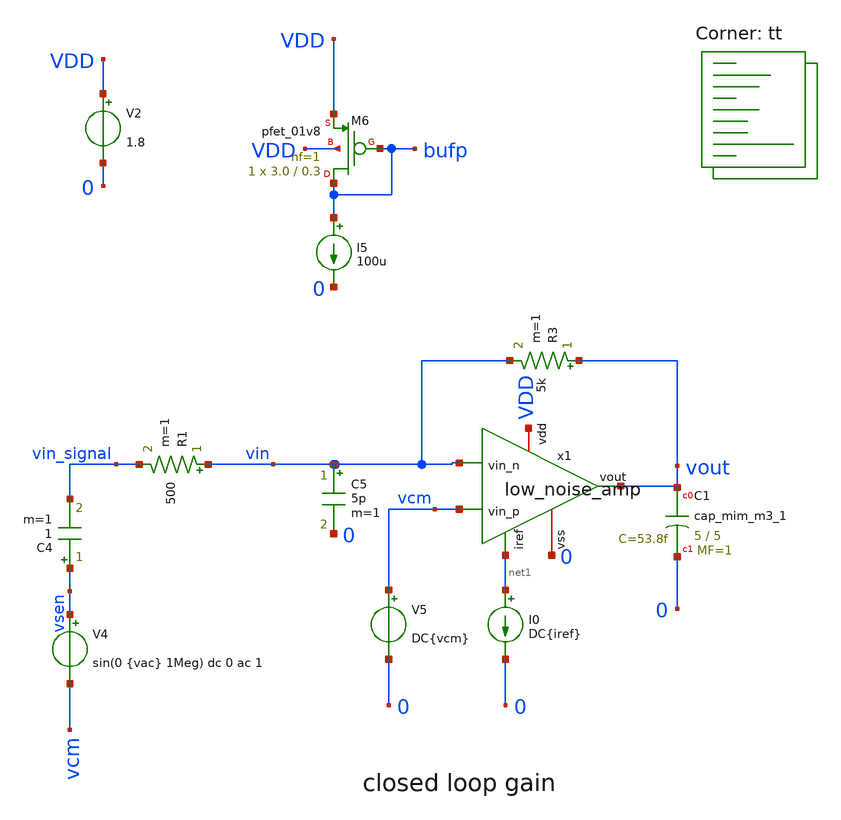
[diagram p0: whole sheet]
** sch_path: design/xschem/low_noise_amp_closed_loop_tb.sch
**.subckt low_noise_amp_closed_loop_tb
V2 VDD 0 1.8
XM6 bufp bufp VDD VDD sky130_fd_pr__pfet_01v8 L=0.3 W=3.0 nf=1 ad='int((nf+1)/2) * W/nf * 0.29' as='int((nf+2)/2) * W/nf * 0.29'
+ pd='2*int((nf+1)/2) * (W/nf + 0.29)' ps='2*int((nf+2)/2) * (W/nf + 0.29)' nrd='0.29 / W' nrs='0.29 / W'
+ sa=0 sb=0 sd=0 mult=1 m=1
I5 bufp 0 100u
XC1 net2 0 sky130_fd_pr__cap_mim_m3_1 W=5 L=5 MF=1 m=1
x1 VDD net1 vin vcm vout 0 low_noise_amp
C5 vin 0 5p m=1
V5 vcm 0 DC{vcm}
V4 vsen vcm sin(0 {vac} 1Meg) dc 0 ac 1
C4 vsen vin_signal 1 m=1
R1 vin vin_signal 500 m=1
R3 vout vin 5k m=1
I0 net1 0 DC{iref}
**** begin user architecture code
.lib $::SKYWATER_MODELS/sky130.lib.spice tt




* Circuit Parameters
.param iref = 100u
.param vdd  = 1.8
.param vss  = 0.0
.param vcm  = 0.8
.param vac  = 10m
.options TEMP = 65.0


* OP Parameters & Singals to save
.save all  @M.X1.XM1.msky130_fd_pr__pfet_01v8[id] @M.X1.XM1.msky130_fd_pr__pfet_01v8[vth] @M.X1.XM1.msky130_fd_pr__pfet_01v8[vgs] @M.X1.XM1.msky130_fd_pr__pfet_01v8[vds] @M.X1.XM1.msky130_fd_pr__pfet_01v8[vdsat] @M.X1.XM1.msky130_fd_pr__pfet_01v8[gm] @M.X1.XM1.msky130_fd_pr__pfet_01v8[gds]  @M.X1.XM2.msky130_fd_pr__pfet_01v8[id] @M.X1.XM2.msky130_fd_pr__pfet_01v8[vth] @M.X1.XM2.msky130_fd_pr__pfet_01v8[vgs] @M.X1.XM2.msky130_fd_pr__pfet_01v8[vds] @M.X1.XM2.msky130_fd_pr__pfet_01v8[vdsat] @M.X1.XM2.msky130_fd_pr__pfet_01v8[gm] @M.X1.XM2.msky130_fd_pr__pfet_01v8[gds]  @M.X1.XM3.msky130_fd_pr__nfet_01v8[id] @M.X1.XM3.msky130_fd_pr__nfet_01v8[vth] @M.X1.XM3.msky130_fd_pr__nfet_01v8[vgs] @M.X1.XM3.msky130_fd_pr__nfet_01v8[vds] @M.X1.XM3.msky130_fd_pr__nfet_01v8[vdsat] @M.X1.XM3.msky130_fd_pr__nfet_01v8[gm] @M.X1.XM3.msky130_fd_pr__nfet_01v8[gds]  @M.X1.XM4.msky130_fd_pr__nfet_01v8[id] @M.X1.XM4.msky130_fd_pr__nfet_01v8[vth] @M.X1.XM4.msky130_fd_pr__nfet_01v8[vgs] @M.X1.XM4.msky130_fd_pr__nfet_01v8[vds] @M.X1.XM4.msky130_fd_pr__nfet_01v8[vdsat] @M.X1.XM4.msky130_fd_pr__nfet_01v8[gm] @M.X1.XM4.msky130_fd_pr__nfet_01v8[gds]  @M.X1.XM5.msky130_fd_pr__pfet_01v8[id] @M.X1.XM5.msky130_fd_pr__pfet_01v8[vth] @M.X1.XM5.msky130_fd_pr__pfet_01v8[vgs] @M.X1.XM5.msky130_fd_pr__pfet_01v8[vds] @M.X1.XM5.msky130_fd_pr__pfet_01v8[vdsat] @M.X1.XM5.msky130_fd_pr__pfet_01v8[gm] @M.X1.XM5.msky130_fd_pr__pfet_01v8[gds]  @M.X1.XM6.msky130_fd_pr__nfet_01v8[id] @M.X1.XM6.msky130_fd_pr__nfet_01v8[vth] @M.X1.XM6.msky130_fd_pr__nfet_01v8[vgs] @M.X1.XM6.msky130_fd_pr__nfet_01v8[vds] @M.X1.XM6.msky130_fd_pr__nfet_01v8[vdsat] @M.X1.XM6.msky130_fd_pr__nfet_01v8[gm] @M.X1.XM6.msky130_fd_pr__nfet_01v8[gds]  @M.X1.XM7.msky130_fd_pr__pfet_01v8[id] @M.X1.XM7.msky130_fd_pr__pfet_01v8[vth] @M.X1.XM7.msky130_fd_pr__pfet_01v8[vgs] @M.X1.XM7.msky130_fd_pr__pfet_01v8[vds] @M.X1.XM7.msky130_fd_pr__pfet_01v8[vdsat] @M.X1.XM7.msky130_fd_pr__pfet_01v8[gm] @M.X1.XM7.msky130_fd_pr__pfet_01v8[gds]  @M.X1.XM8.msky130_fd_pr__pfet_01v8[id] @M.X1.XM8.msky130_fd_pr__pfet_01v8[vth] @M.X1.XM8.msky130_fd_pr__pfet_01v8[vgs] @M.X1.XM8.msky130_fd_pr__pfet_01v8[vds] @M.X1.XM8.msky130_fd_pr__pfet_01v8[vdsat] @M.X1.XM8.msky130_fd_pr__pfet_01v8[gm] @M.X1.XM8.msky130_fd_pr__pfet_01v8[gds]  @M.X1.XM9.msky130_fd_pr__nfet_01v8[id] @M.X1.XM9.msky130_fd_pr__nfet_01v8[vth] @M.X1.XM9.msky130_fd_pr__nfet_01v8[vgs] @M.X1.XM9.msky130_fd_pr__nfet_01v8[vds] @M.X1.XM9.msky130_fd_pr__nfet_01v8[vdsat] @M.X1.XM9.msky130_fd_pr__nfet_01v8[gm] @M.X1.XM9.msky130_fd_pr__nfet_01v8[gds]

*Simulations
.control
  ac dec 200 0.1 10G
  setplot ac1
  meas ac GBW when vdb(vout)=0
  meas ac DCG find vdb(vout) at=1k
  *meas ac PM find vp(vout) when vdb(vout)=0
  *print PM*180/PI
  *meas ac GM find vdb(vout) when vp(vout)=0
  plot vdb(vout) {vp(vout)*180/PI}
  write opamp_closeloop_ac1.raw

  reset
  tran 0.01u 11u
  setplot tran1
  plot v(vsen) v(vout)
  write opamp_closeloop_tran1.raw

  reset
  noise v(vout) V4 dec 200 0.1 10G 1
  setplot noise1
  plot inoise_spectrum onoise_spectrum
  *print inoise_spectrum
  *print onoise_spectrum
  setplot noise2
  *plot inoise_total onoise_total
  print inoise_total
  print onoise_total
  write opamp_closeloop_noise.raw

  reset
  op
  setplot op1
  print vout
  write opamp_closeloop_op1.raw

.endc

.end


**** end user architecture code
**.ends
.end
